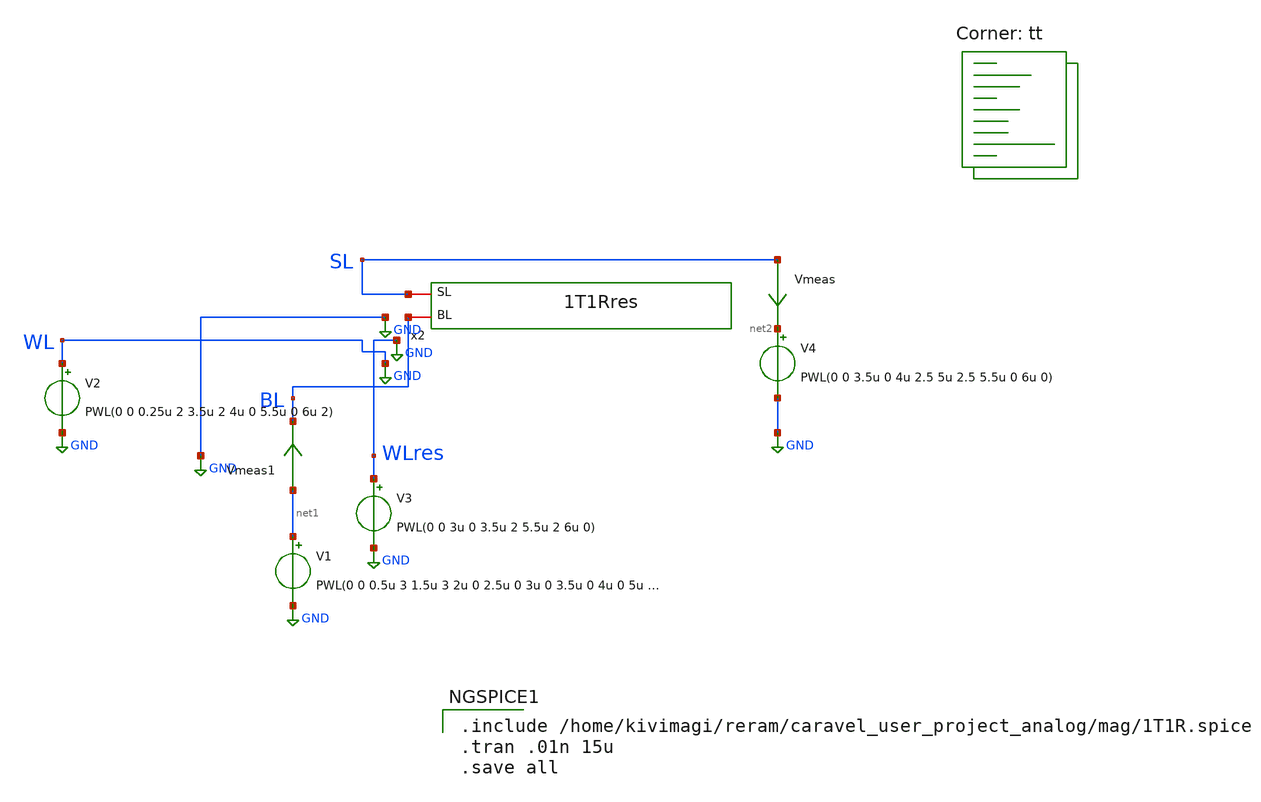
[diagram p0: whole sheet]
** sch_path: xschem/Crossbar/1t1rTB.sch
**.subckt 1t1rTB
Vmeas SL net2 0
.save i(vmeas)
V2 WL GND PWL(0 0 0.25u 2 3.5u 2 4u 0 5.5u 0 6u 2)
Vmeas1 net1 BL 0
.save i(vmeas1)
V1 net1 GND PWL(0 0 0.5u 3 1.5u 3 2u 0 2.5u 0 3u 0 3.5u 0 4u 0 5u 0 5.5u 0 6u 0.2 7u 0.2)
V3 WLres GND PWL(0 0 3u 0 3.5u 2 5.5u 2 6u 0)
V4 net2 GND PWL(0 0 3.5u 0 4u 2.5 5u 2.5 5.5u 0 6u 0)
x2 BL SL 1T1Rres
**** begin user architecture code
.lib $::SKYWATER_MODELS/sky130.lib.spice tt

.include /home/kivimagi/reram/caravel_user_project_analog/mag/1T1R.spice
.tran .01n 15u
.save all


**** end user architecture code
**.ends
.GLOBAL GND
.end
